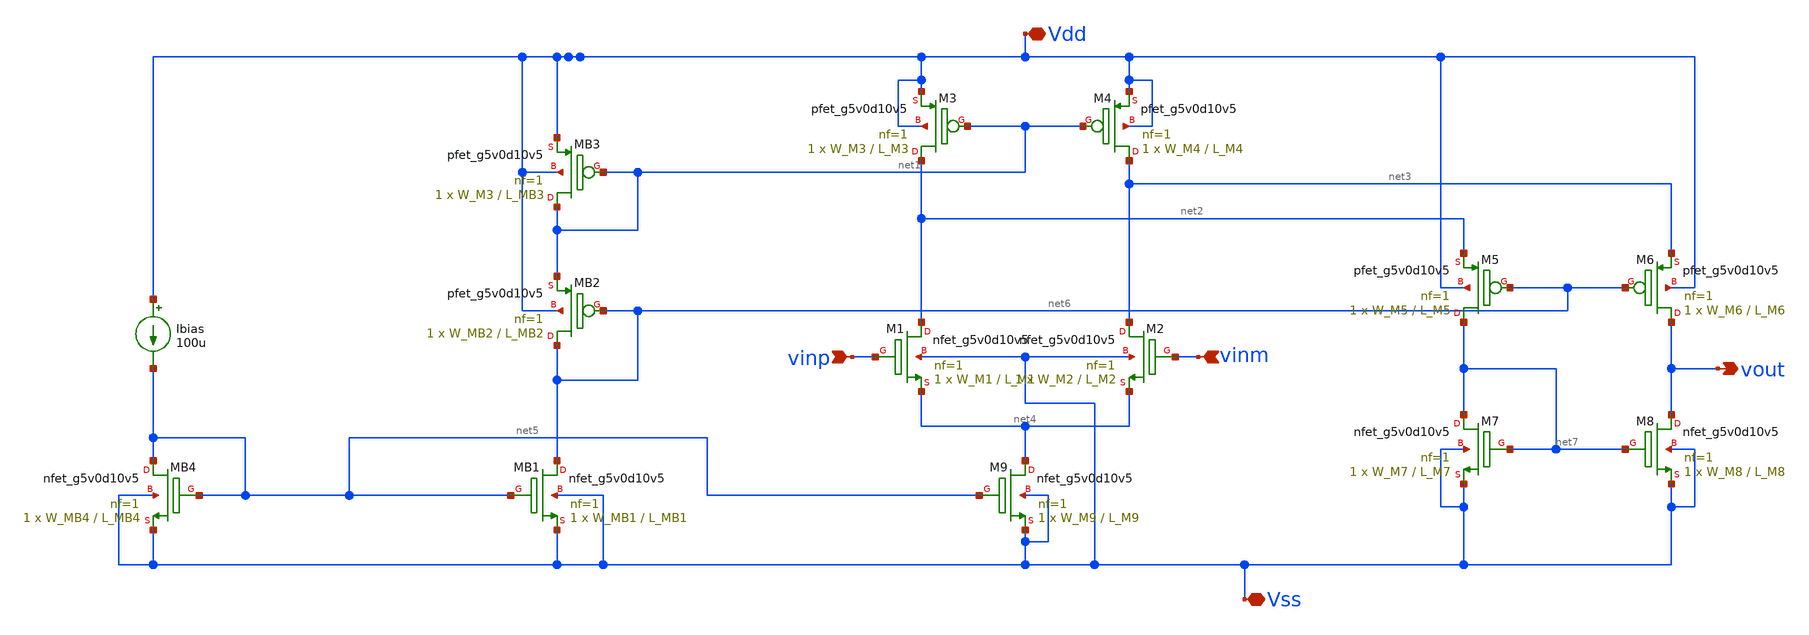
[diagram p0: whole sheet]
** sch_path: xschem/diff_pair_folded_cascode2.sch
**.subckt diff_pair_folded_cascode2 Vdd vinm vinp Vss vout
*.iopin Vdd
*.ipin vinm
*.ipin vinp
*.iopin Vss
*.opin vout
XM1 net2 vinp net4 Vss sky130_fd_pr__nfet_g5v0d10v5 L=L_M1 W=W_M1 nf=1 ad='int((nf+1)/2) * W/nf * 0.29'
+ as='int((nf+2)/2) * W/nf * 0.29' pd='2*int((nf+1)/2) * (W/nf + 0.29)' ps='2*int((nf+2)/2) * (W/nf + 0.29)'
+ nrd='0.29 / W' nrs='0.29 / W' sa=0 sb=0 sd=0 mult=1 m=1
XM2 net3 vinm net4 Vss sky130_fd_pr__nfet_g5v0d10v5 L=L_M2 W=W_M2 nf=1 ad='int((nf+1)/2) * W/nf * 0.29'
+ as='int((nf+2)/2) * W/nf * 0.29' pd='2*int((nf+1)/2) * (W/nf + 0.29)' ps='2*int((nf+2)/2) * (W/nf + 0.29)'
+ nrd='0.29 / W' nrs='0.29 / W' sa=0 sb=0 sd=0 mult=1 m=1
XM4 net3 net1 Vdd Vdd sky130_fd_pr__pfet_g5v0d10v5 L=L_M4 W=W_M4 nf=1 ad='int((nf+1)/2) * W/nf * 0.29'
+ as='int((nf+2)/2) * W/nf * 0.29' pd='2*int((nf+1)/2) * (W/nf + 0.29)' ps='2*int((nf+2)/2) * (W/nf + 0.29)'
+ nrd='0.29 / W' nrs='0.29 / W' sa=0 sb=0 sd=0 mult=1 m=1
XM3 net2 net1 Vdd Vdd sky130_fd_pr__pfet_g5v0d10v5 L=L_M3 W=W_M3 nf=1 ad='int((nf+1)/2) * W/nf * 0.29'
+ as='int((nf+2)/2) * W/nf * 0.29' pd='2*int((nf+1)/2) * (W/nf + 0.29)' ps='2*int((nf+2)/2) * (W/nf + 0.29)'
+ nrd='0.29 / W' nrs='0.29 / W' sa=0 sb=0 sd=0 mult=1 m=1
XM9 net4 net5 Vss Vss sky130_fd_pr__nfet_g5v0d10v5 L=L_M9 W=W_M9 nf=1 ad='int((nf+1)/2) * W/nf * 0.29'
+ as='int((nf+2)/2) * W/nf * 0.29' pd='2*int((nf+1)/2) * (W/nf + 0.29)' ps='2*int((nf+2)/2) * (W/nf + 0.29)'
+ nrd='0.29 / W' nrs='0.29 / W' sa=0 sb=0 sd=0 mult=1 m=1
XM6 vout net6 net3 Vdd sky130_fd_pr__pfet_g5v0d10v5 L=L_M6 W=W_M6 nf=1 ad='int((nf+1)/2) * W/nf * 0.29'
+ as='int((nf+2)/2) * W/nf * 0.29' pd='2*int((nf+1)/2) * (W/nf + 0.29)' ps='2*int((nf+2)/2) * (W/nf + 0.29)'
+ nrd='0.29 / W' nrs='0.29 / W' sa=0 sb=0 sd=0 mult=1 m=1
XM5 net7 net6 net2 Vdd sky130_fd_pr__pfet_g5v0d10v5 L=L_M5 W=W_M5 nf=1 ad='int((nf+1)/2) * W/nf * 0.29'
+ as='int((nf+2)/2) * W/nf * 0.29' pd='2*int((nf+1)/2) * (W/nf + 0.29)' ps='2*int((nf+2)/2) * (W/nf + 0.29)'
+ nrd='0.29 / W' nrs='0.29 / W' sa=0 sb=0 sd=0 mult=1 m=1
XM7 net7 net7 Vss Vss sky130_fd_pr__nfet_g5v0d10v5 L=L_M7 W=W_M7 nf=1 ad='int((nf+1)/2) * W/nf * 0.29'
+ as='int((nf+2)/2) * W/nf * 0.29' pd='2*int((nf+1)/2) * (W/nf + 0.29)' ps='2*int((nf+2)/2) * (W/nf + 0.29)'
+ nrd='0.29 / W' nrs='0.29 / W' sa=0 sb=0 sd=0 mult=1 m=1
XM8 vout net7 Vss Vss sky130_fd_pr__nfet_g5v0d10v5 L=L_M8 W=W_M8 nf=1 ad='int((nf+1)/2) * W/nf * 0.29'
+ as='int((nf+2)/2) * W/nf * 0.29' pd='2*int((nf+1)/2) * (W/nf + 0.29)' ps='2*int((nf+2)/2) * (W/nf + 0.29)'
+ nrd='0.29 / W' nrs='0.29 / W' sa=0 sb=0 sd=0 mult=1 m=1
XMB3 net1 net1 Vdd Vdd sky130_fd_pr__pfet_g5v0d10v5 L=L_MB3 W=W_M3 nf=1 ad='int((nf+1)/2) * W/nf * 0.29'
+ as='int((nf+2)/2) * W/nf * 0.29' pd='2*int((nf+1)/2) * (W/nf + 0.29)' ps='2*int((nf+2)/2) * (W/nf + 0.29)'
+ nrd='0.29 / W' nrs='0.29 / W' sa=0 sb=0 sd=0 mult=1 m=1
XMB1 net6 net5 Vss Vss sky130_fd_pr__nfet_g5v0d10v5 L=L_MB1 W=W_MB1 nf=1 ad='int((nf+1)/2) * W/nf * 0.29'
+ as='int((nf+2)/2) * W/nf * 0.29' pd='2*int((nf+1)/2) * (W/nf + 0.29)' ps='2*int((nf+2)/2) * (W/nf + 0.29)'
+ nrd='0.29 / W' nrs='0.29 / W' sa=0 sb=0 sd=0 mult=1 m=1
XMB2 net6 net6 net1 Vdd sky130_fd_pr__pfet_g5v0d10v5 L=L_MB2 W=W_MB2 nf=1 ad='int((nf+1)/2) * W/nf * 0.29'
+ as='int((nf+2)/2) * W/nf * 0.29' pd='2*int((nf+1)/2) * (W/nf + 0.29)' ps='2*int((nf+2)/2) * (W/nf + 0.29)'
+ nrd='0.29 / W' nrs='0.29 / W' sa=0 sb=0 sd=0 mult=1 m=1
XMB4 net5 net5 Vss Vss sky130_fd_pr__nfet_g5v0d10v5 L=L_MB4 W=W_MB4 nf=1 ad='int((nf+1)/2) * W/nf * 0.29'
+ as='int((nf+2)/2) * W/nf * 0.29' pd='2*int((nf+1)/2) * (W/nf + 0.29)' ps='2*int((nf+2)/2) * (W/nf + 0.29)'
+ nrd='0.29 / W' nrs='0.29 / W' sa=0 sb=0 sd=0 mult=1 m=1
Ibias Vdd net5 100u
**.ends
.end
